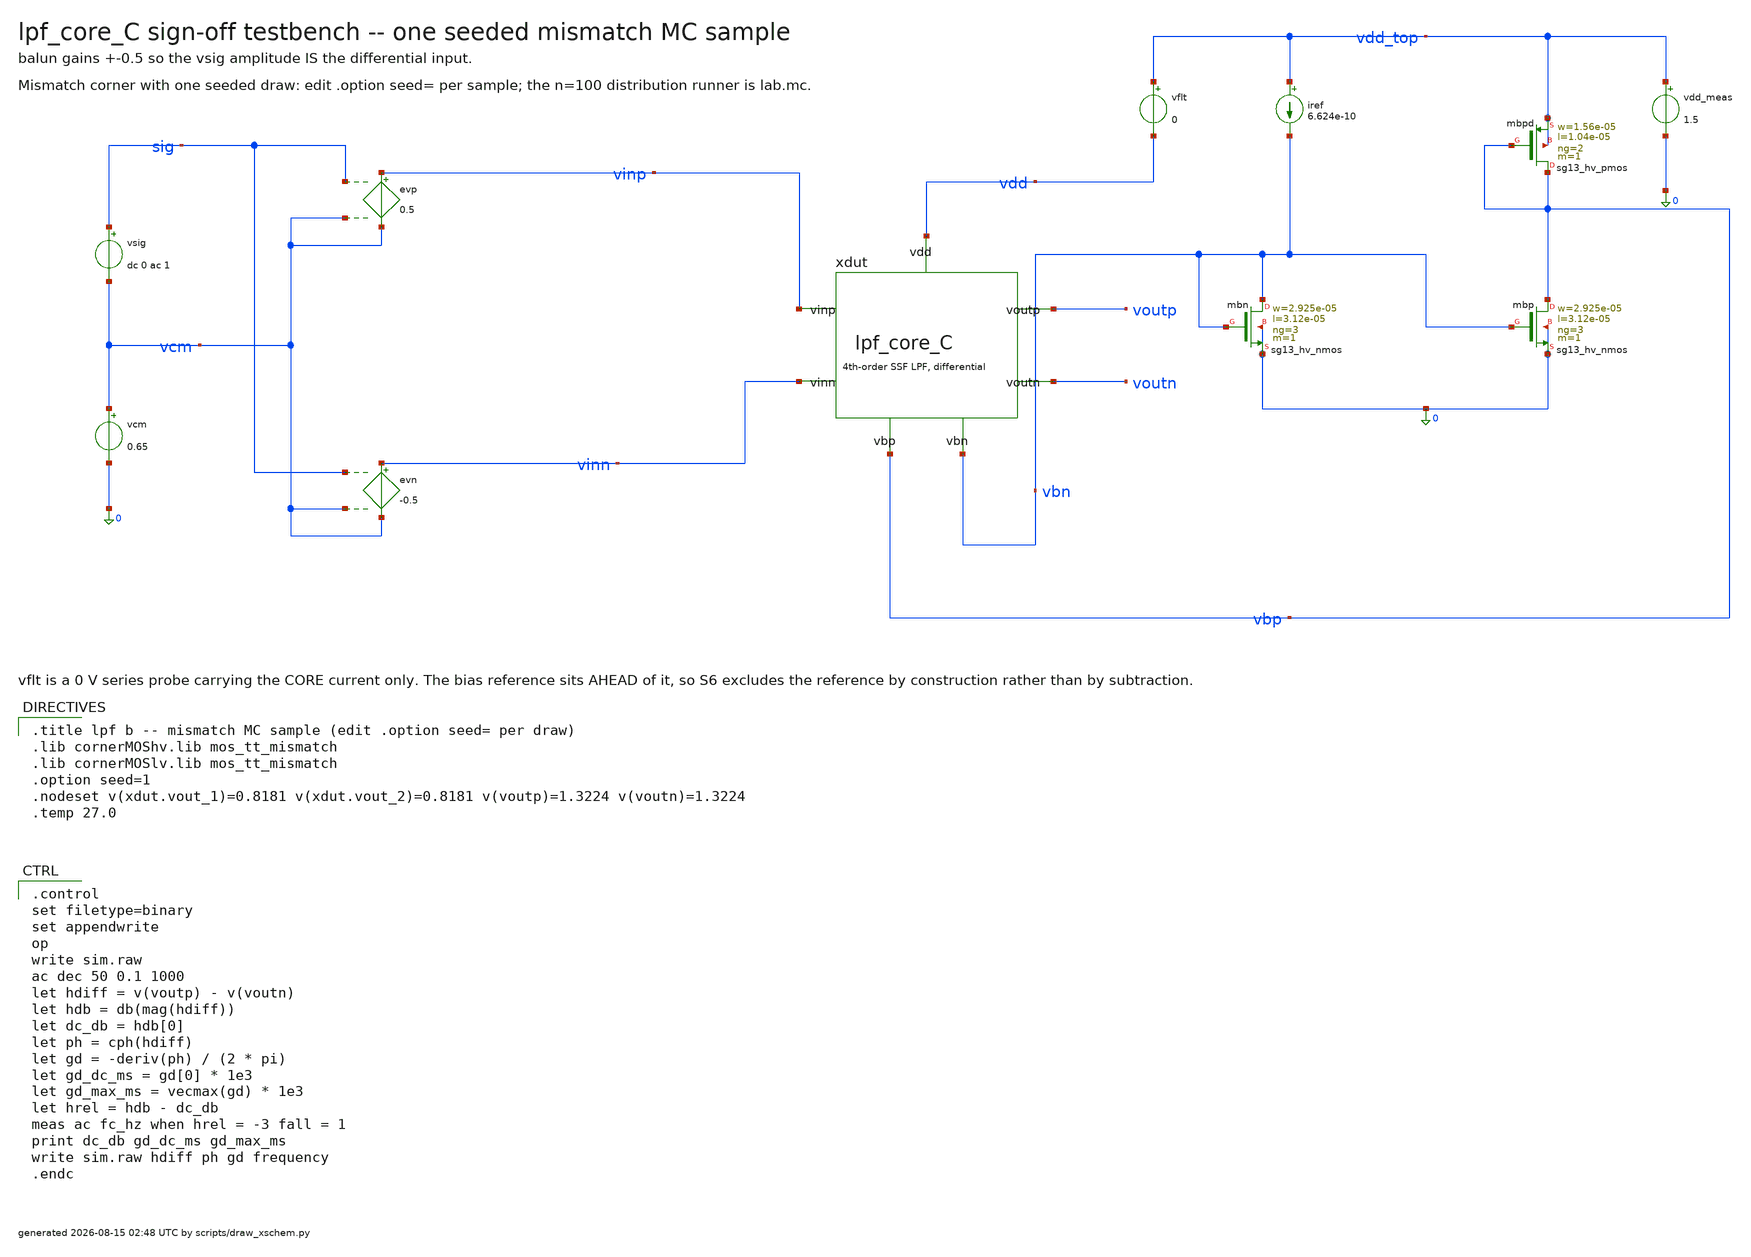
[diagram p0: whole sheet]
** sch_path: signoff/C-lownoise/lpf_tb_C_mc.sch
**.subckt lpf_tb_C_mc
vsig sig vcm dc 0 ac 1
vcm vcm 0 0.65
evp vinp vcm sig vcm 0.5
evn vinn vcm sig vcm -0.5
xdut vinp vinn voutp voutn vbn vbp vdd lpf_core_C
vflt vdd_top vdd 0
vdd_meas vdd_top 0 1.5
iref vdd_top vbn 6.624e-10
Xmbn vbn vbn 0 0 sg13_hv_nmos w=2.925e-05 l=3.12e-05 ng=3 m=1 mm_ok=1
Xmbp vbp vbn 0 0 sg13_hv_nmos w=2.925e-05 l=3.12e-05 ng=3 m=1 mm_ok=1
Xmbpd vbp vbp vdd_top vdd_top sg13_hv_pmos w=1.56e-05 l=1.04e-05 ng=2 m=1 mm_ok=1
**** begin user architecture code

.title lpf b -- mismatch MC sample (edit .option seed= per draw)
.lib cornerMOShv.lib mos_tt_mismatch
.lib cornerMOSlv.lib mos_tt_mismatch
.option seed=1
.nodeset v(xdut.vout_1)=0.8181 v(xdut.vout_2)=0.8181 v(voutp)=1.3224 v(voutn)=1.3224
.temp 27.0


.control
set filetype=binary
set appendwrite
op
write sim.raw
ac dec 50 0.1 1000
let hdiff = v(voutp) - v(voutn)
let hdb = db(mag(hdiff))
let dc_db = hdb[0]
let ph = cph(hdiff)
let gd = -deriv(ph) / (2 * pi)
let gd_dc_ms = gd[0] * 1e3
let gd_max_ms = vecmax(gd) * 1e3
let hrel = hdb - dc_db
meas ac fc_hz when hrel = -3 fall = 1
print dc_db gd_dc_ms gd_max_ms
write sim.raw hdiff ph gd frequency
.endc

**** end user architecture code
**.ends
.end
